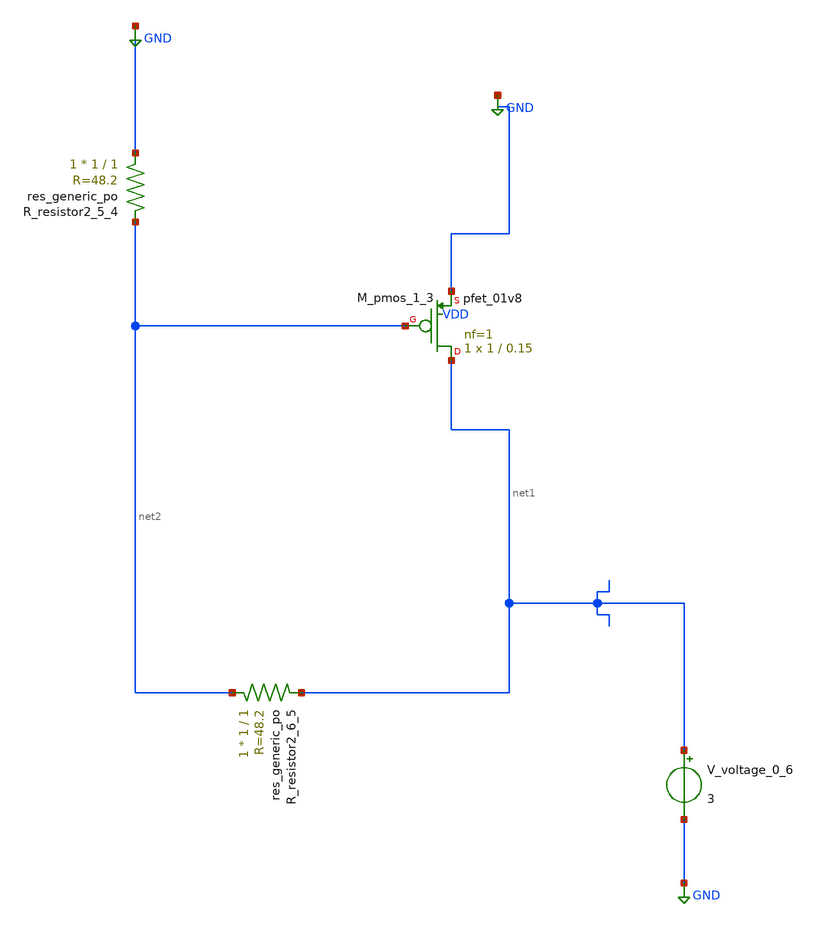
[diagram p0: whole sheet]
** sch_path: schematics/AMSNet/284.sch
**.subckt 284
XM_pmos_1_3 net1 net2 GND VDD sky130_fd_pr__pfet_01v8 L=0.15 W=1 nf=1 ad='int((1 + 1)/2) * 1 / 1 * 0.29'
+ as='int((1 + 2)/2) * 1 / 1 * 0.29' pd='2*int((1 + 1)/2) * (1 / 1 + 0.29)' ps='2*int((1 + 2)/2) * (1 / 1 + 0.29)'
+ nrd='0.29 / 1 ' nrs='0.29 / 1 ' sa=0 sb=0 sd=0 mult=1 m=1
XR_resistor2_5_4 GND net2 sky130_fd_pr__res_generic_po W=1 L=1 m=1
XR_resistor2_6_5 net2 net1 sky130_fd_pr__res_generic_po W=1 L=1 m=1
V_voltage_0_6 net1 GND 3
**.ends
.GLOBAL GND
.end
